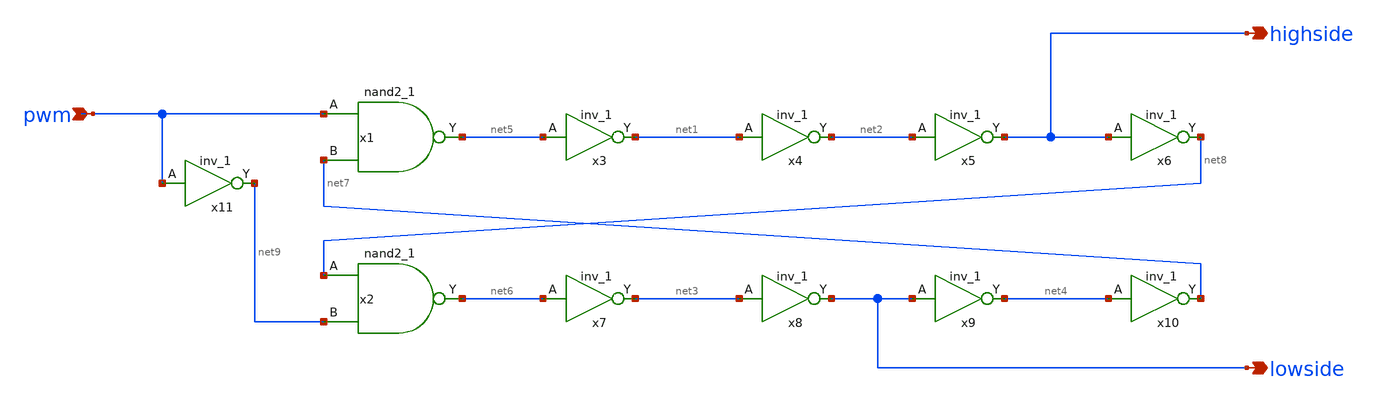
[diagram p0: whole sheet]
** sch_path: Ene_Thompson/deadtime.sch
**.subckt deadtime pwm highside lowside
*.ipin pwm
*.opin highside
*.opin lowside
x1 pwm net7 VGND VNB VPB VPWR net5 sky130_fd_sc_hd__nand2_1
x2 net8 net9 VGND VNB VPB VPWR net6 sky130_fd_sc_hd__nand2_1
x3 net5 VGND VNB VPB VPWR net1 sky130_fd_sc_hd__inv_1
x4 net1 VGND VNB VPB VPWR net2 sky130_fd_sc_hd__inv_1
x5 net2 VGND VNB VPB VPWR highside sky130_fd_sc_hd__inv_1
x6 highside VGND VNB VPB VPWR net8 sky130_fd_sc_hd__inv_1
x7 net6 VGND VNB VPB VPWR net3 sky130_fd_sc_hd__inv_1
x8 net3 VGND VNB VPB VPWR lowside sky130_fd_sc_hd__inv_1
x9 lowside VGND VNB VPB VPWR net4 sky130_fd_sc_hd__inv_1
x10 net4 VGND VNB VPB VPWR net7 sky130_fd_sc_hd__inv_1
x11 pwm VGND VNB VPB VPWR net9 sky130_fd_sc_hd__inv_1
**.ends
.end
